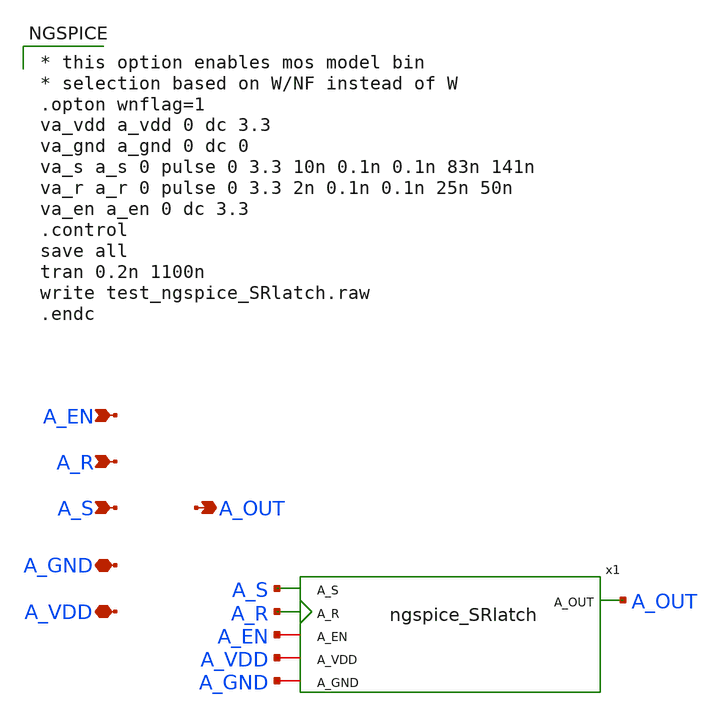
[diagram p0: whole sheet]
** sch_path: xschem/test_ngspice_SRlatch.sch
**.subckt test_ngspice_SRlatch A_VDD A_S A_GND A_R A_OUT A_EN
*.iopin A_VDD
*.ipin A_S
*.iopin A_GND
*.ipin A_R
*.opin A_OUT
*.ipin A_EN
x1 A_OUT A_S A_R A_EN A_GND A_VDD ngspice_SRlatch
**** begin user architecture code

* this option enables mos model bin
* selection based on W/NF instead of W
.opton wnflag=1
va_vdd a_vdd 0 dc 3.3
va_gnd a_gnd 0 dc 0
va_s a_s 0 pulse 0 3.3 10n 0.1n 0.1n 83n 141n
va_r a_r 0 pulse 0 3.3 2n 0.1n 0.1n 25n 50n
va_en a_en 0 dc 3.3
.control
save all
tran 0.2n 1100n
write test_ngspice_SRlatch.raw
.endc


**** end user architecture code
**.ends

* expanding   symbol:  /foss/designs/TO202406_CMOSVCO_Esm22/xschem/ngspice_SRlatch.sym # of pins=6
** sym_path: xschem/ngspice_SRlatch.sym
** sch_path: xschem/ngspice_SRlatch.sch
.subckt ngspice_SRlatch A_OUT A_S A_R A_EN A_GND A_VDD
*.iopin A_VDD
*.ipin A_S
*.opin A_OUT
*.ipin A_R
*.ipin A_EN
*.iopin A_GND
* noconn A_VDD
* noconn A_S
* noconn A_R
* noconn A_GND
* noconn A_OUT
* noconn A_EN
**** begin user architecture code
.model todig_3v3 adc_bridge(in_high=2.2 in_low=1.1  rise_delay=2n fall_delay=2n)
.model toana_3v3 dac_bridge(out_high=3.3 out_low=0)

.model dsrflop d_srlatch(ic=0 rise_delay=1n fall_delay=1n)

AA2D1 [A_GND] [d_gnd] todig_3v3

AA2D2 [A_S] [d_s] todig_3v3
AA2D3 [A_R] [d_r] todig_3v3
AA2D4 [A_EN] [d_en] todig_3v3

A1 d_s d_r d_en d_gnd d_gnd d_out NULL dsrflop

AD2A1 [d_out] [A_OUT] toana_3v3

**** end user architecture code
.ends

.end
